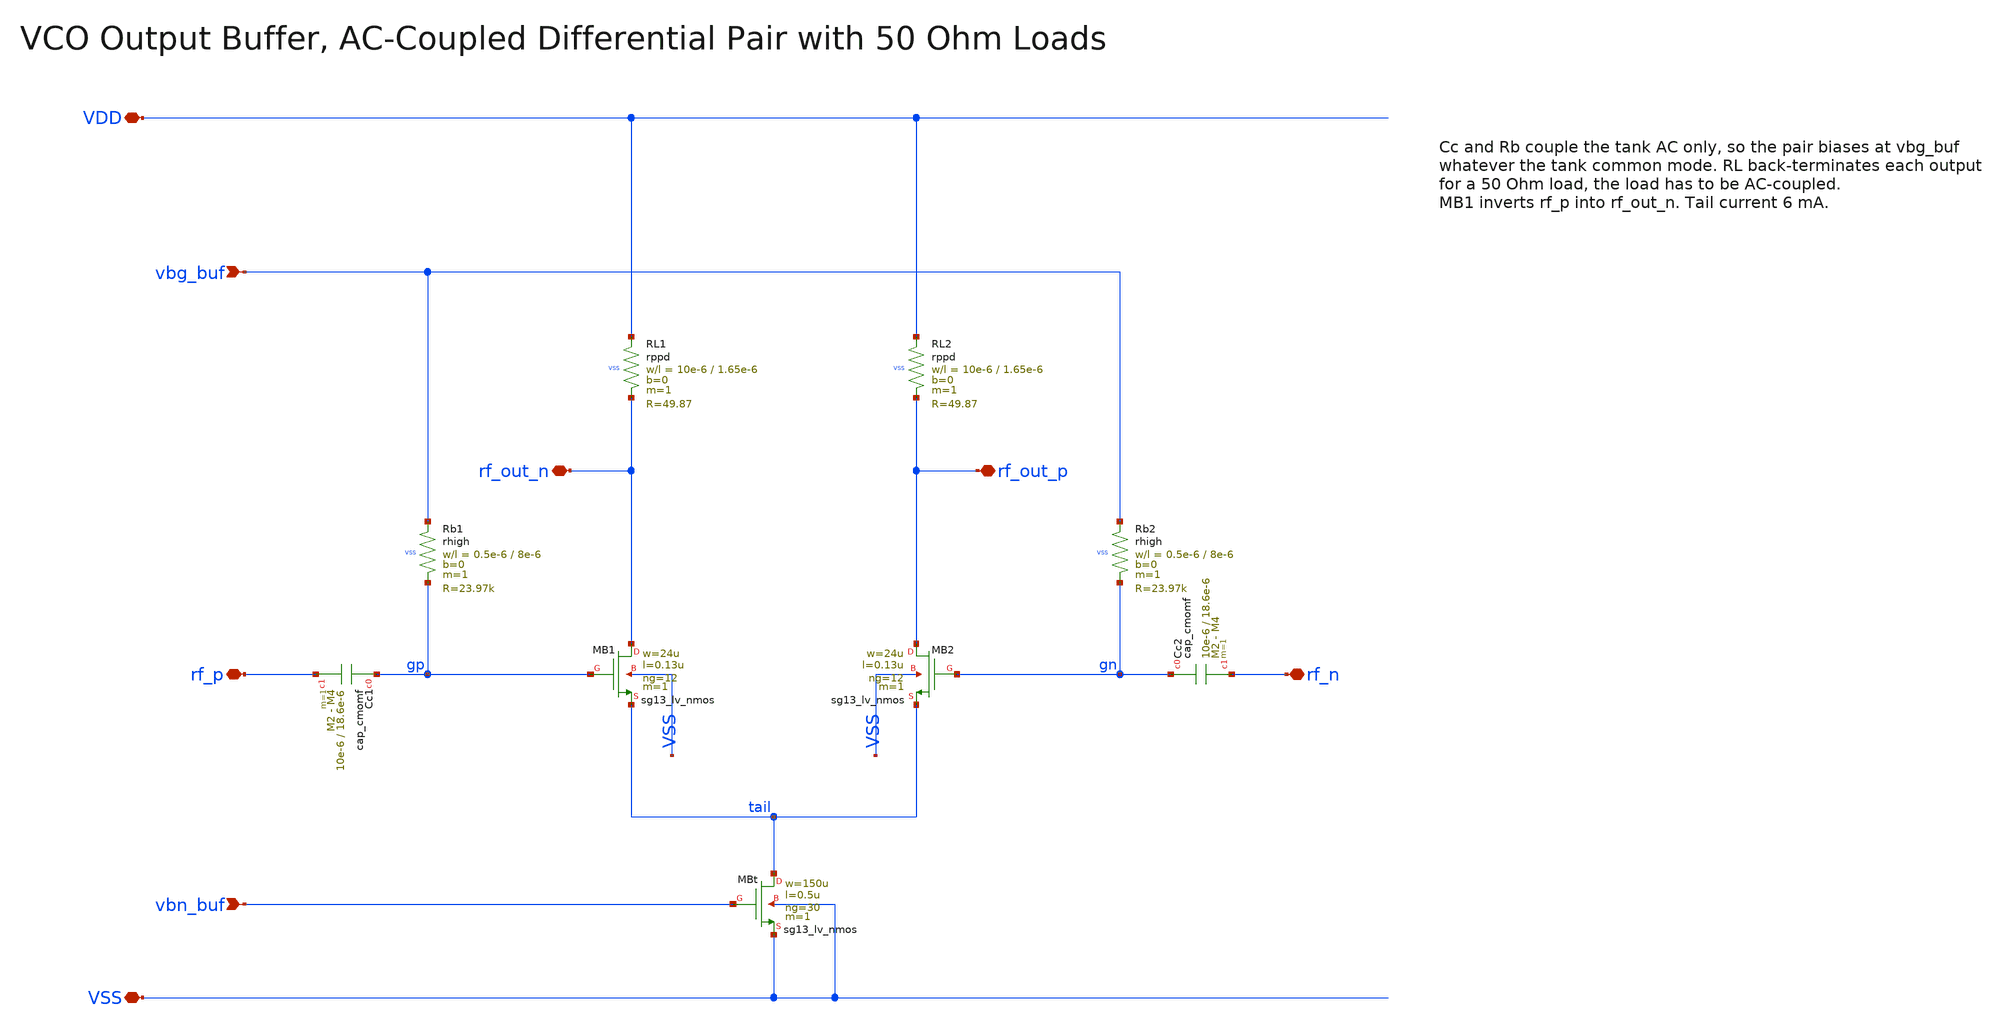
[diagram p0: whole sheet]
** sch_path: macros/vco/schematic/xschem/vco_buf.sch
**.subckt vco_buf VDD VSS rf_out_n rf_out_p vbn_buf rf_p rf_n vbg_buf
*.iopin VDD
*.iopin VSS
*.iopin rf_out_n
*.iopin rf_out_p
*.ipin vbn_buf
*.iopin rf_p
*.iopin rf_n
*.ipin vbg_buf
XMB1 rf_out_n gp tail VSS sg13_lv_nmos w=24u l=0.13u ng=12 m=1 mm_ok=1
XMB2 rf_out_p gn tail VSS sg13_lv_nmos w=24u l=0.13u ng=12 m=1 mm_ok=1
XRL1 VDD rf_out_n VSS rppd w=10e-6 l=1.65e-6 m=1 b=0 mm_ok=1
XRL2 VDD rf_out_p VSS rppd w=10e-6 l=1.65e-6 m=1 b=0 mm_ok=1
XMBt tail vbn_buf VSS VSS sg13_lv_nmos w=150u l=0.5u ng=30 m=1 mm_ok=1
XCc1 gp rf_p cap_cmomf w=10e-6 l=18.6e-6 mmin=2 mmax=4 subblock=0 rfmodel=0 subscale=1 m=1 mm_ok=1
XCc2 gn rf_n cap_cmomf w=10e-6 l=18.6e-6 mmin=2 mmax=4 subblock=0 rfmodel=0 subscale=1 m=1 mm_ok=1
XRb1 vbg_buf gp VSS rhigh w=0.5e-6 l=8e-6 m=1 b=0 mm_ok=1
XRb2 vbg_buf gn VSS rhigh w=0.5e-6 l=8e-6 m=1 b=0 mm_ok=1
**.ends
.end
